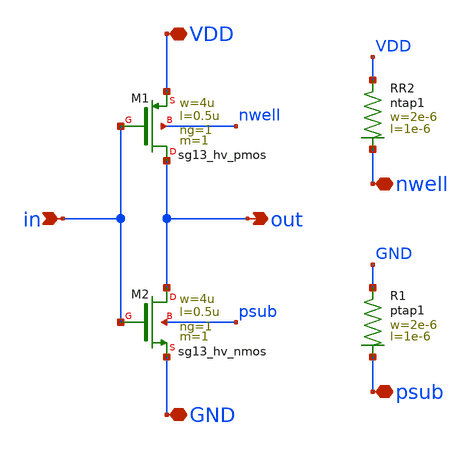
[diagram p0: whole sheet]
** sch_path: xschem/inv.sch
**.subckt inv in GND out VDD nwell psub
*.ipin in
*.iopin GND
*.opin out
*.iopin VDD
*.iopin nwell
*.iopin psub
XM1 out in VDD nwell sg13_hv_pmos w=4u l=0.5u ng=1 m=1 mm_ok=1
XM2 out in GND psub sg13_hv_nmos w=4u l=0.5u ng=1 m=1 mm_ok=1
XR1 GND psub ptap1 R=122.5 w=2e-6 l=1e-6
XR2 VDD nwell ntap1 R=122.5 w=2e-6 l=1e-6
**.ends
.end
